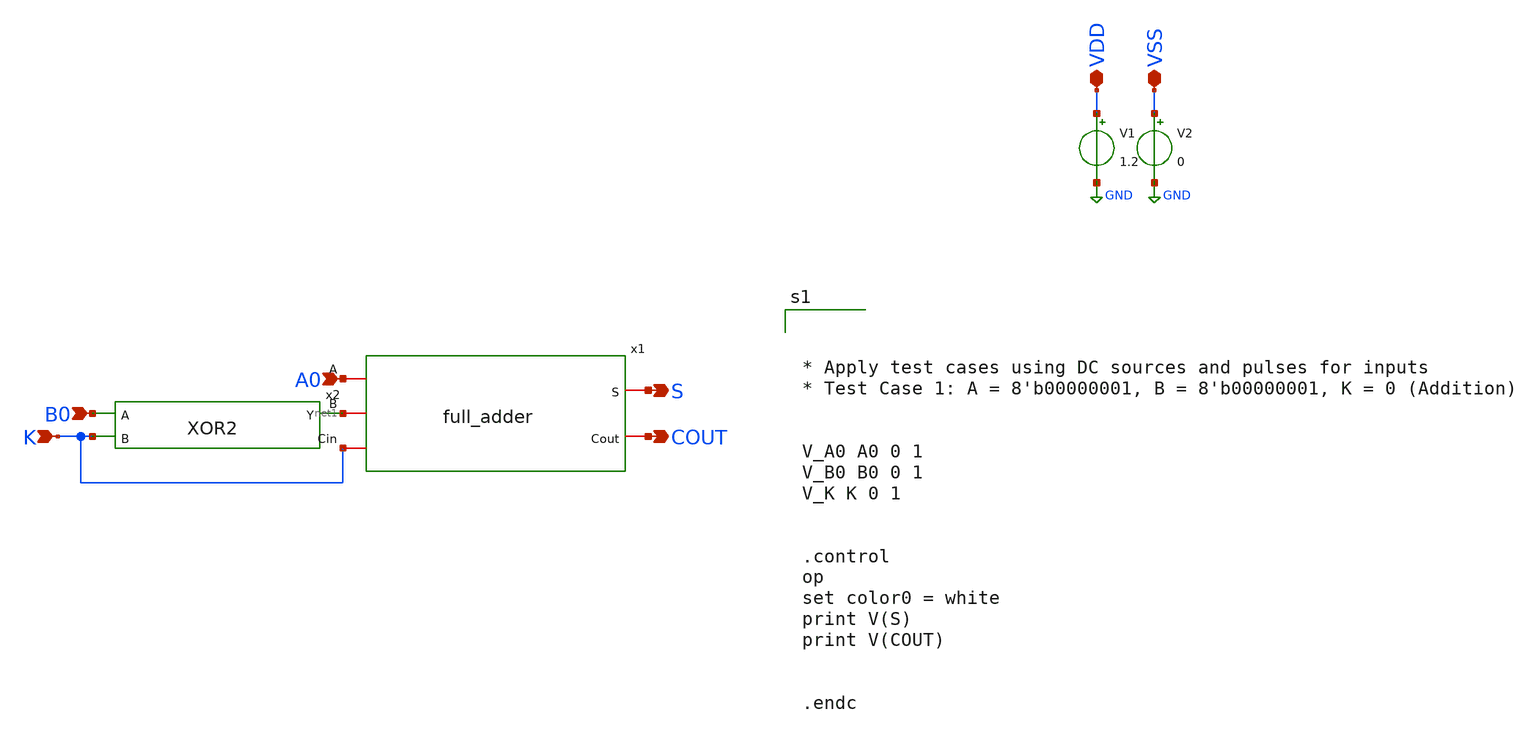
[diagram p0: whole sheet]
** sch_path: design/xschem/TEST_BENCHES/subs_adder_TB.sch
**.subckt subs_adder_TB VDD VSS A0 B0 S COUT K
*.iopin VDD
*.iopin VSS
*.ipin A0
*.ipin B0
*.opin S
*.opin COUT
*.ipin K
x1 A0 S net1 K COUT full_adder
V1 VDD GND 1.2
V2 VSS GND 0
x2 B0 K net1 VSS VDD XOR2
**** begin user architecture code

** opencircuitdesign pdks install
.lib $::SKYWATER_MODELS/sky130.lib.spice tt_mm





* Apply test cases using DC sources and pulses for inputs
* Test Case 1: A = 8'b00000001, B = 8'b00000001, K = 0 (Addition)


V_A0 A0 0 1
V_B0 B0 0 1
V_K K 0 1


.control
op
set color0 = white
print V(S)
print V(COUT)


.endc


**** end user architecture code
**.ends
.GLOBAL GND
.end
